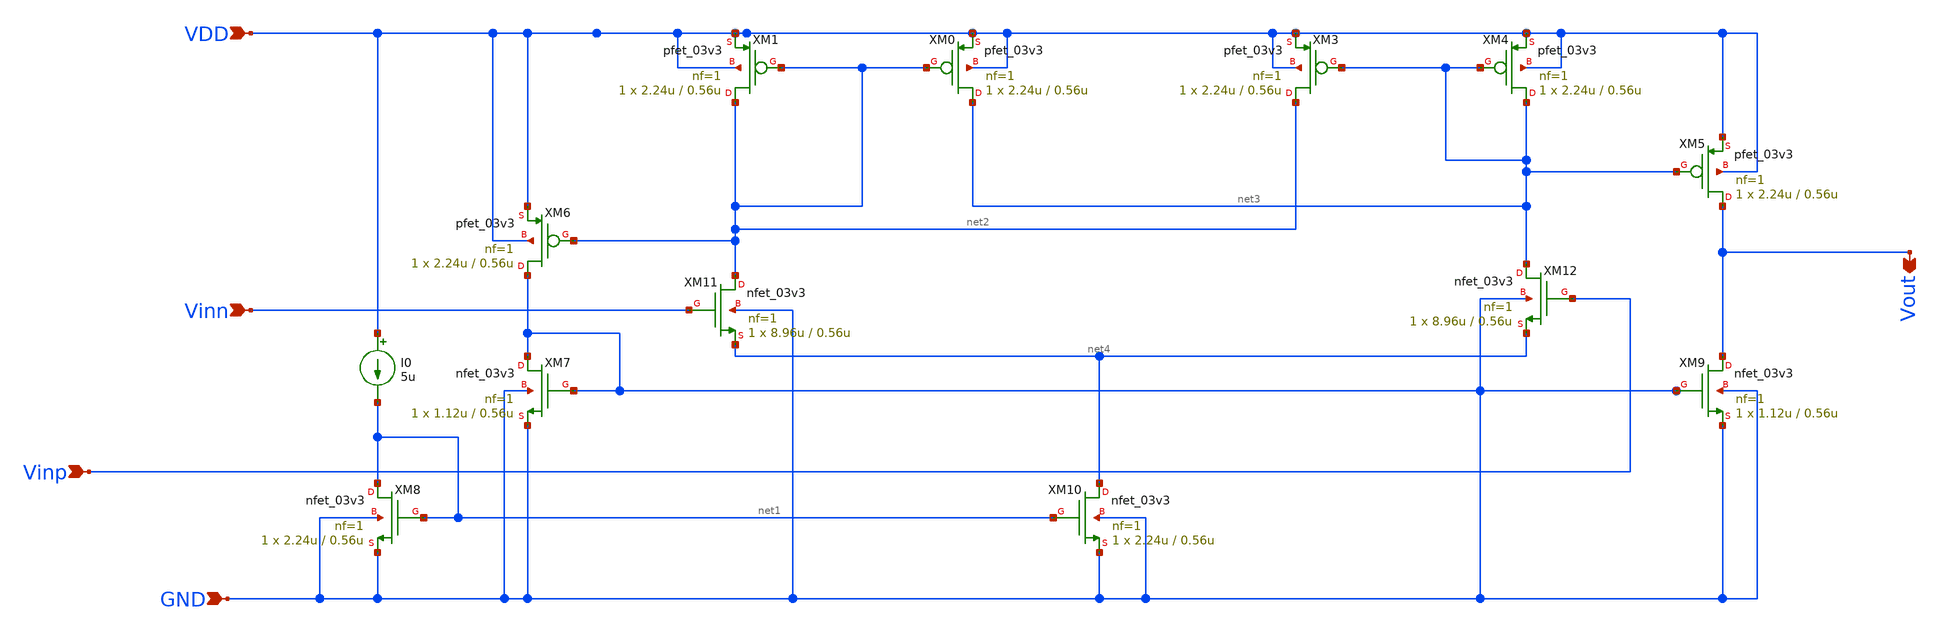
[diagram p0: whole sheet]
** sch_path: comparator/schematic-design/comp_forsym.sch
**.subckt comp_forsym Vout Vinn Vinp VDD GND
*.opin Vout
*.ipin Vinn
*.ipin Vinp
*.ipin VDD
*.ipin GND
XM1 net2 net2 VDD VDD pfet_03v3 L=0.56u W=2.24u nf=1 ad='int((nf+1)/2) * W/nf * 0.18u' as='int((nf+2)/2) * W/nf * 0.18u'
+ pd='2*int((nf+1)/2) * (W/nf + 0.18u)' ps='2*int((nf+2)/2) * (W/nf + 0.18u)' nrd='0.18u / W' nrs='0.18u / W'
+ sa=0 sb=0 sd=0 m=1
XM0 net3 net2 VDD VDD pfet_03v3 L=0.56u W=2.24u nf=1 ad='int((nf+1)/2) * W/nf * 0.18u' as='int((nf+2)/2) * W/nf * 0.18u'
+ pd='2*int((nf+1)/2) * (W/nf + 0.18u)' ps='2*int((nf+2)/2) * (W/nf + 0.18u)' nrd='0.18u / W' nrs='0.18u / W'
+ sa=0 sb=0 sd=0 m=1
XM3 net2 net3 VDD VDD pfet_03v3 L=0.56u W=2.24u nf=1 ad='int((nf+1)/2) * W/nf * 0.18u' as='int((nf+2)/2) * W/nf * 0.18u'
+ pd='2*int((nf+1)/2) * (W/nf + 0.18u)' ps='2*int((nf+2)/2) * (W/nf + 0.18u)' nrd='0.18u / W' nrs='0.18u / W'
+ sa=0 sb=0 sd=0 m=1
XM4 net3 net3 VDD VDD pfet_03v3 L=0.56u W=2.24u nf=1 ad='int((nf+1)/2) * W/nf * 0.18u' as='int((nf+2)/2) * W/nf * 0.18u'
+ pd='2*int((nf+1)/2) * (W/nf + 0.18u)' ps='2*int((nf+2)/2) * (W/nf + 0.18u)' nrd='0.18u / W' nrs='0.18u / W'
+ sa=0 sb=0 sd=0 m=1
XM5 Vout net3 VDD VDD pfet_03v3 L=0.56u W=2.24u nf=1 ad='int((nf+1)/2) * W/nf * 0.18u' as='int((nf+2)/2) * W/nf * 0.18u'
+ pd='2*int((nf+1)/2) * (W/nf + 0.18u)' ps='2*int((nf+2)/2) * (W/nf + 0.18u)' nrd='0.18u / W' nrs='0.18u / W'
+ sa=0 sb=0 sd=0 m=1
XM6 GND net2 VDD VDD pfet_03v3 L=0.56u W=2.24u nf=1 ad='int((nf+1)/2) * W/nf * 0.18u' as='int((nf+2)/2) * W/nf * 0.18u'
+ pd='2*int((nf+1)/2) * (W/nf + 0.18u)' ps='2*int((nf+2)/2) * (W/nf + 0.18u)' nrd='0.18u / W' nrs='0.18u / W'
+ sa=0 sb=0 sd=0 m=1
XM7 GND GND GND GND nfet_03v3 L=0.56u W=1.12u nf=1 ad='int((nf+1)/2) * W/nf * 0.18u' as='int((nf+2)/2) * W/nf * 0.18u'
+ pd='2*int((nf+1)/2) * (W/nf + 0.18u)' ps='2*int((nf+2)/2) * (W/nf + 0.18u)' nrd='0.18u / W' nrs='0.18u / W'
+ sa=0 sb=0 sd=0 m=1
XM8 net1 net1 GND GND nfet_03v3 L=0.56u W=2.24u nf=1 ad='int((nf+1)/2) * W/nf * 0.18u' as='int((nf+2)/2) * W/nf * 0.18u'
+ pd='2*int((nf+1)/2) * (W/nf + 0.18u)' ps='2*int((nf+2)/2) * (W/nf + 0.18u)' nrd='0.18u / W' nrs='0.18u / W'
+ sa=0 sb=0 sd=0 m=1
XM9 Vout GND GND GND nfet_03v3 L=0.56u W=1.12u nf=1 ad='int((nf+1)/2) * W/nf * 0.18u' as='int((nf+2)/2) * W/nf * 0.18u'
+ pd='2*int((nf+1)/2) * (W/nf + 0.18u)' ps='2*int((nf+2)/2) * (W/nf + 0.18u)' nrd='0.18u / W' nrs='0.18u / W'
+ sa=0 sb=0 sd=0 m=1
XM10 net4 net1 GND GND nfet_03v3 L=0.56u W=2.24u nf=1 ad='int((nf+1)/2) * W/nf * 0.18u' as='int((nf+2)/2) * W/nf * 0.18u'
+ pd='2*int((nf+1)/2) * (W/nf + 0.18u)' ps='2*int((nf+2)/2) * (W/nf + 0.18u)' nrd='0.18u / W' nrs='0.18u / W'
+ sa=0 sb=0 sd=0 m=1
XM11 net2 Vinn net4 GND nfet_03v3 L=0.56u W=8.96u nf=1 ad='int((nf+1)/2) * W/nf * 0.18u' as='int((nf+2)/2) * W/nf * 0.18u'
+ pd='2*int((nf+1)/2) * (W/nf + 0.18u)' ps='2*int((nf+2)/2) * (W/nf + 0.18u)' nrd='0.18u / W' nrs='0.18u / W'
+ sa=0 sb=0 sd=0 m=1
XM12 net3 Vinp net4 GND nfet_03v3 L=0.56u W=8.96u nf=1 ad='int((nf+1)/2) * W/nf * 0.18u' as='int((nf+2)/2) * W/nf * 0.18u'
+ pd='2*int((nf+1)/2) * (W/nf + 0.18u)' ps='2*int((nf+2)/2) * (W/nf + 0.18u)' nrd='0.18u / W' nrs='0.18u / W'
+ sa=0 sb=0 sd=0 m=1
I0 VDD net1 5u
**.ends
.end
